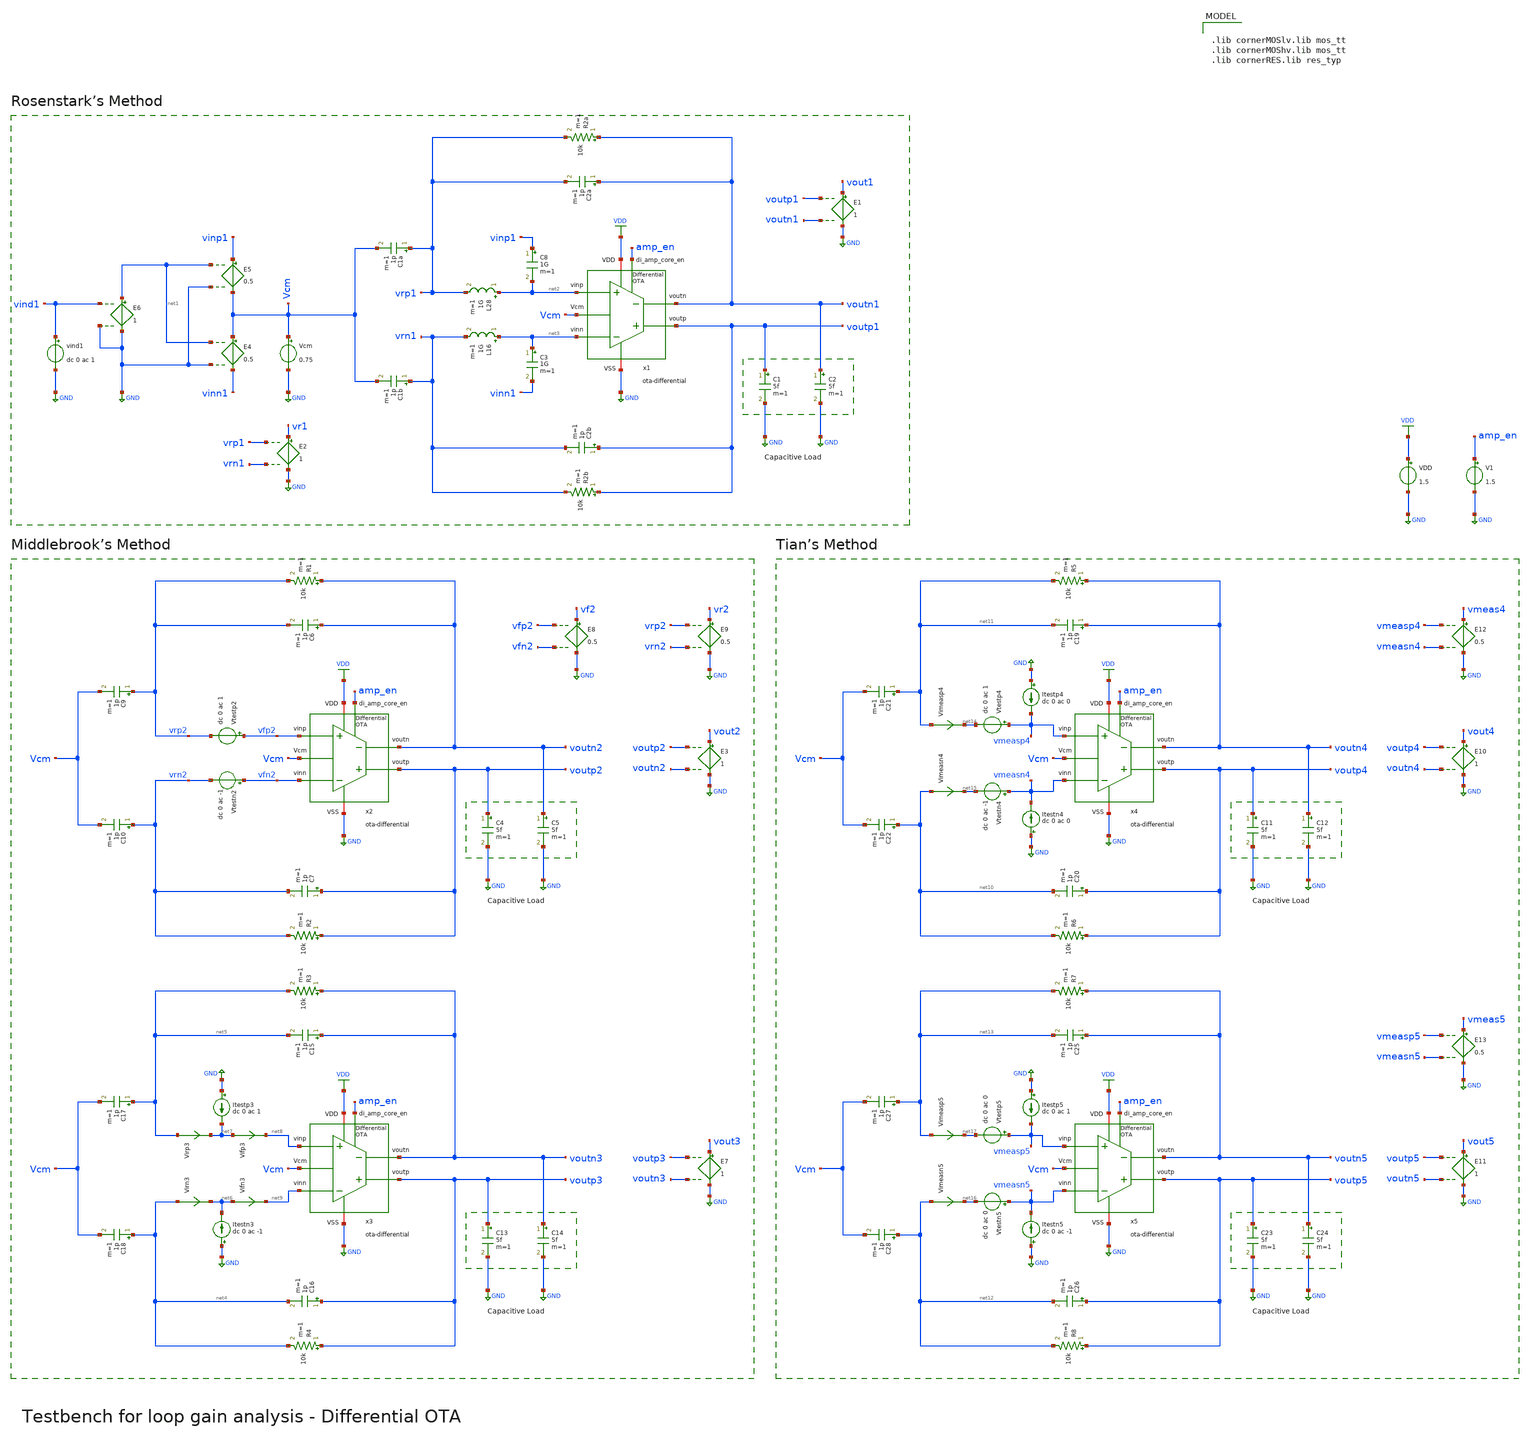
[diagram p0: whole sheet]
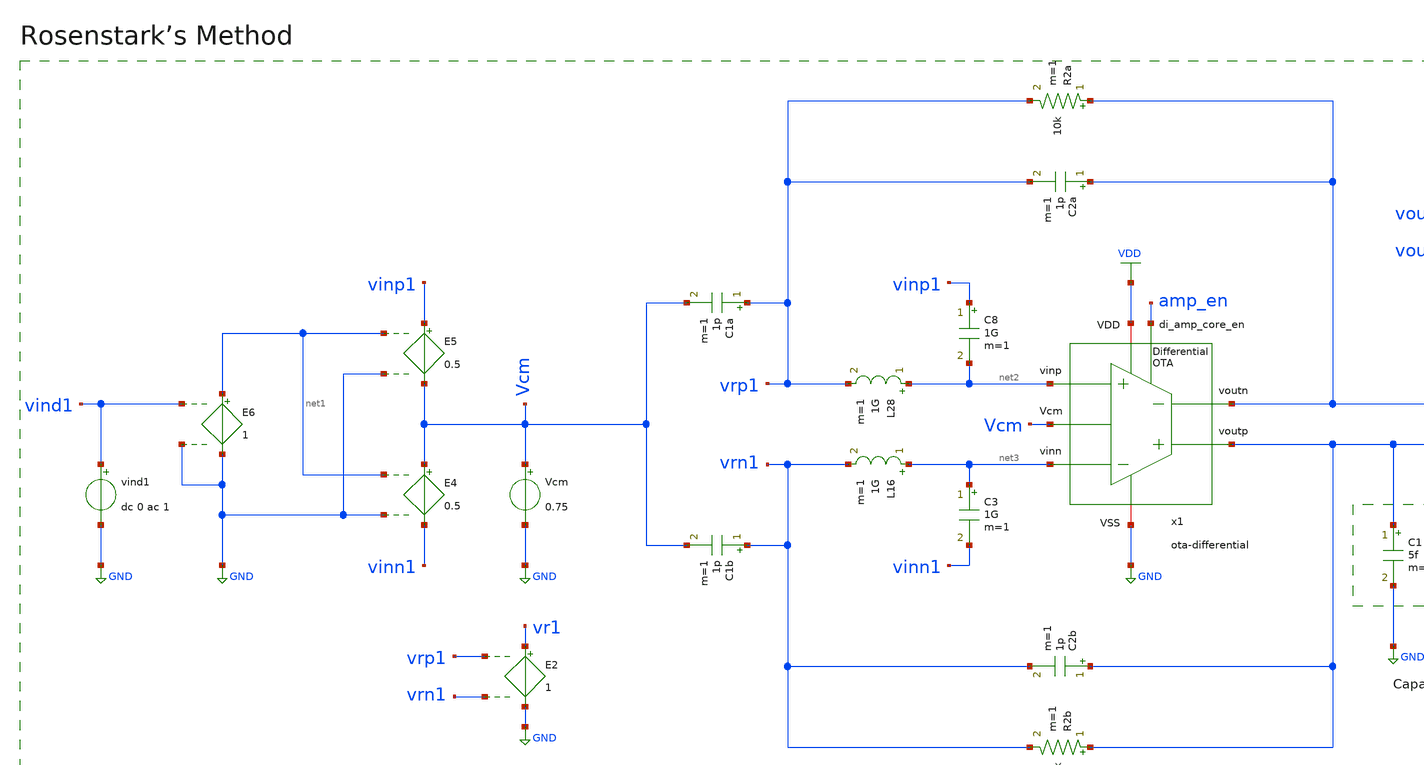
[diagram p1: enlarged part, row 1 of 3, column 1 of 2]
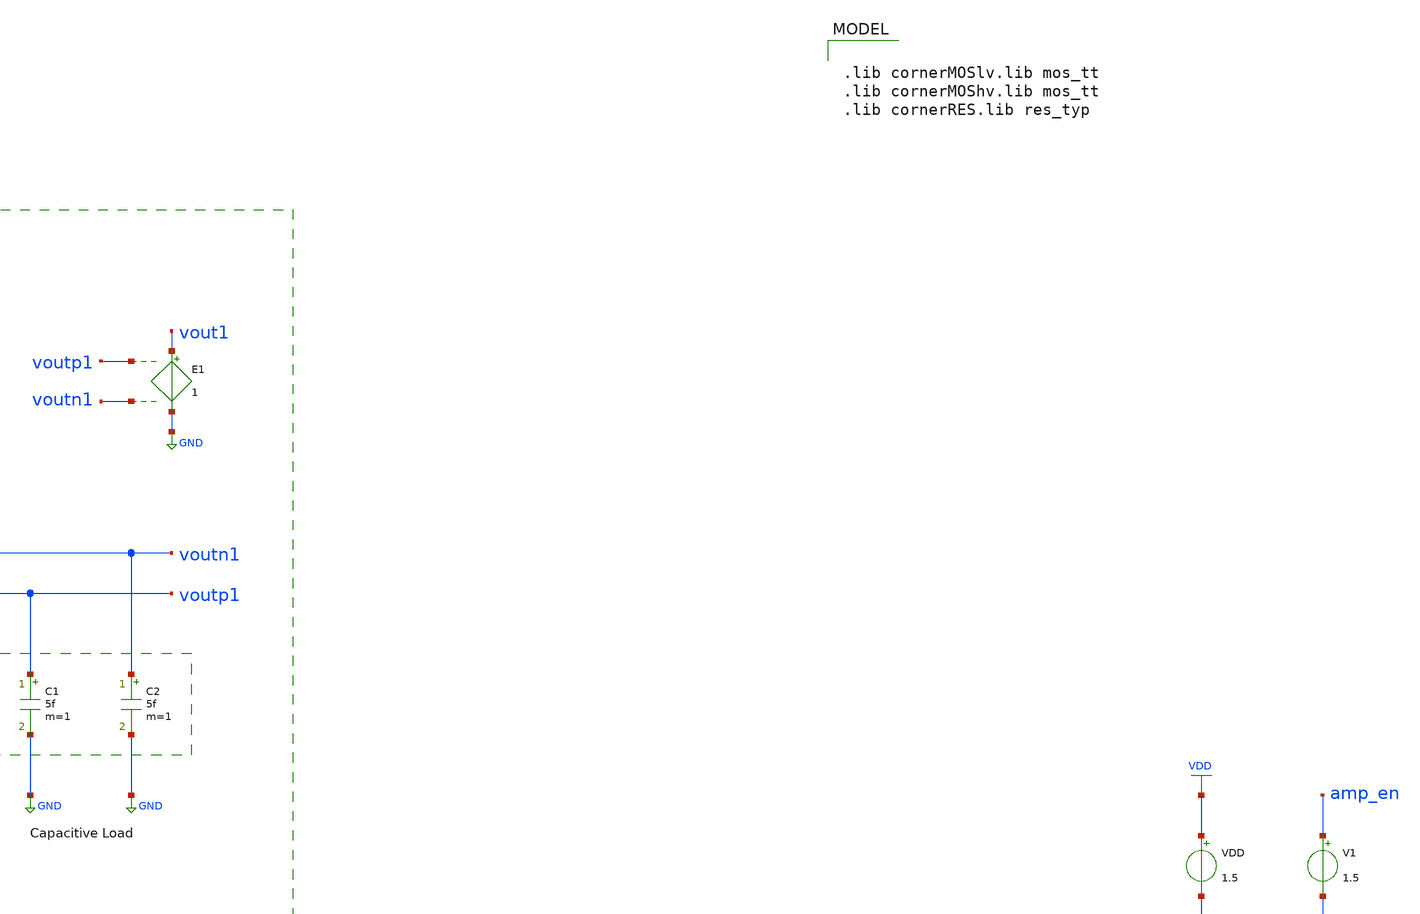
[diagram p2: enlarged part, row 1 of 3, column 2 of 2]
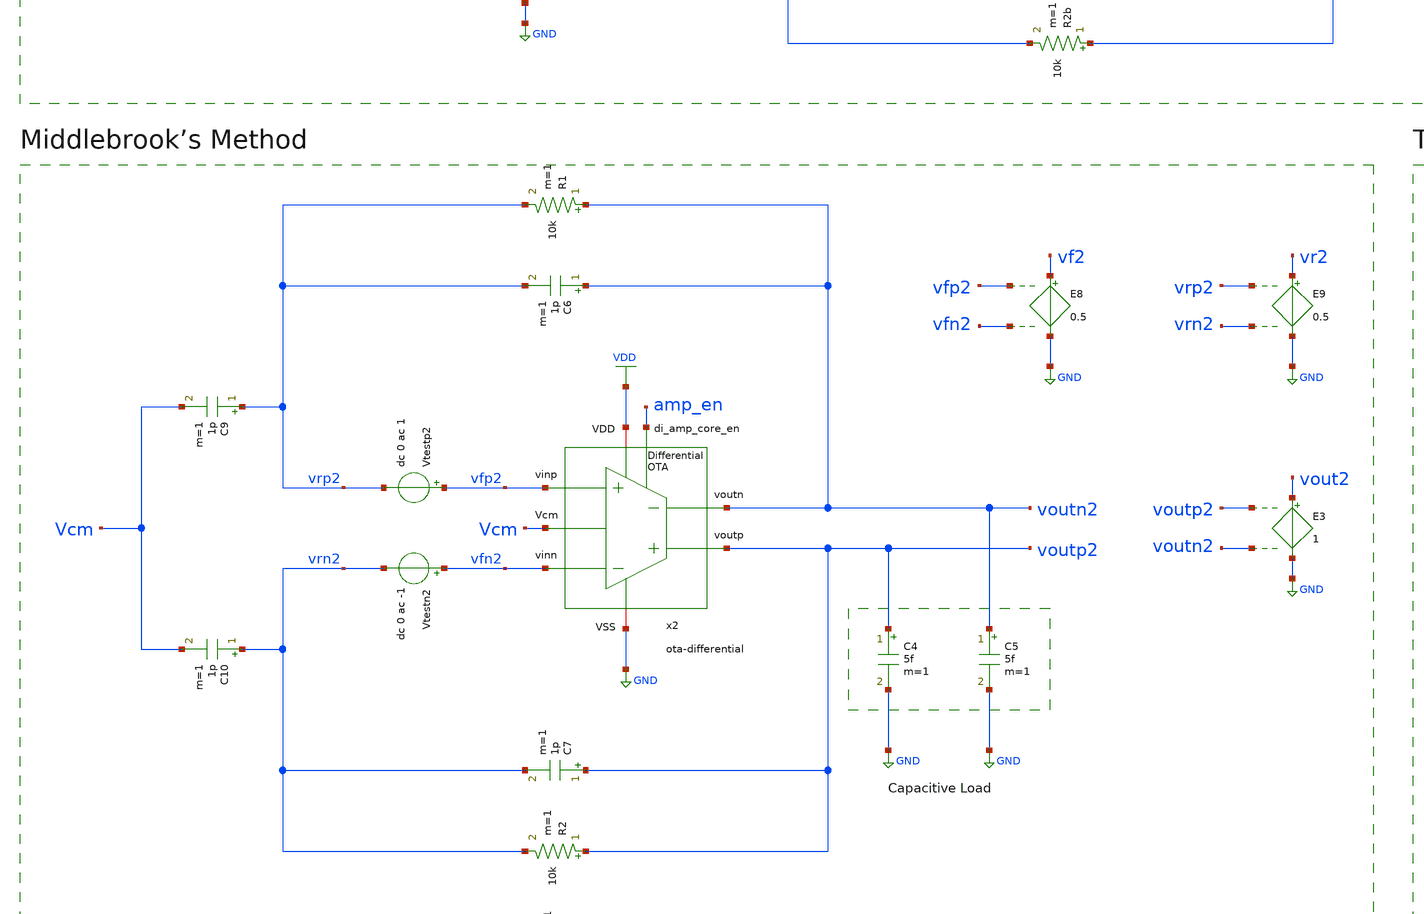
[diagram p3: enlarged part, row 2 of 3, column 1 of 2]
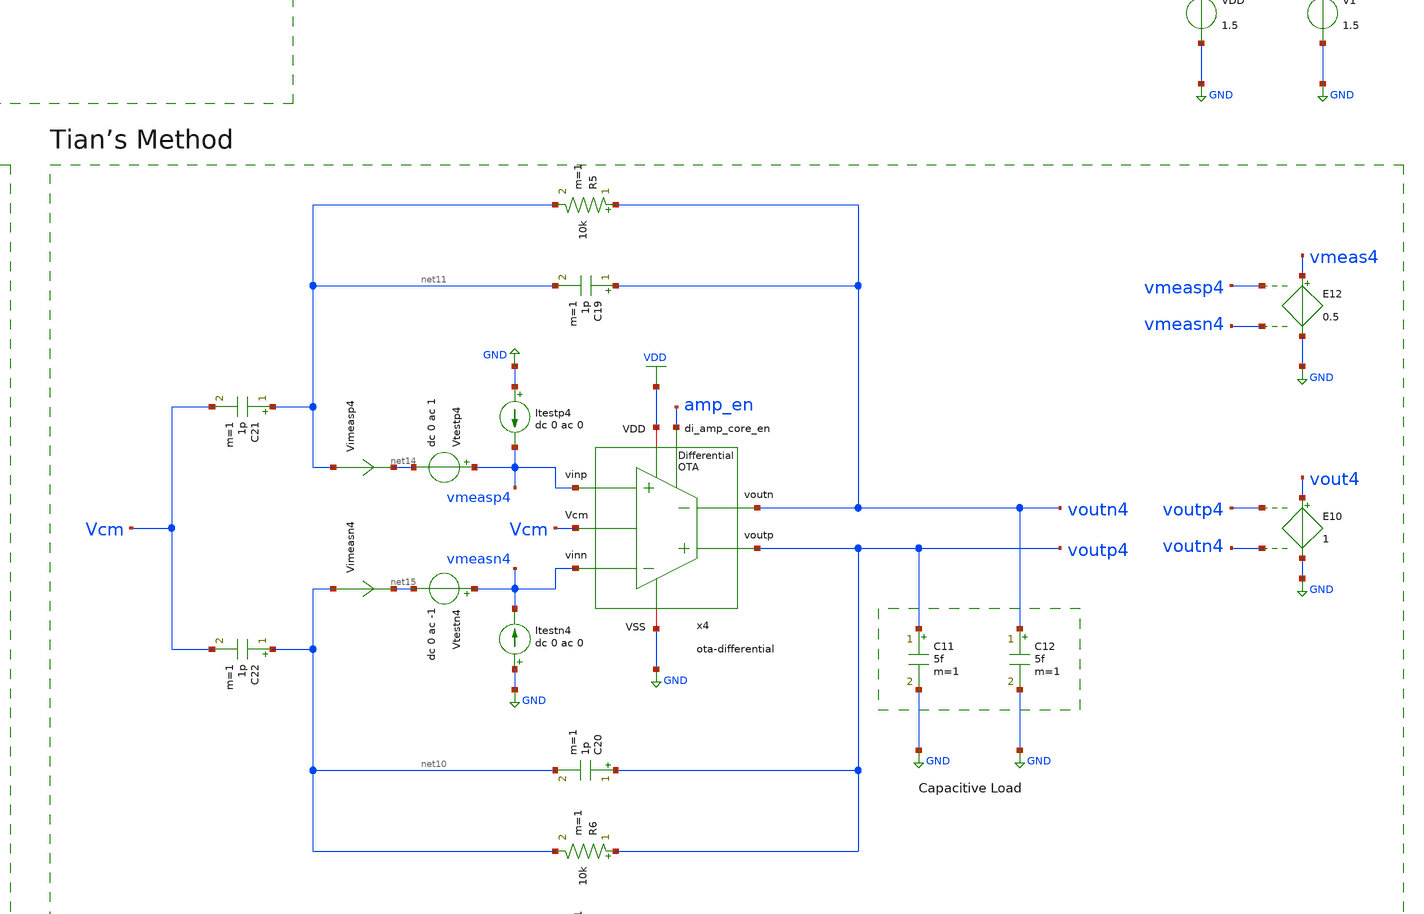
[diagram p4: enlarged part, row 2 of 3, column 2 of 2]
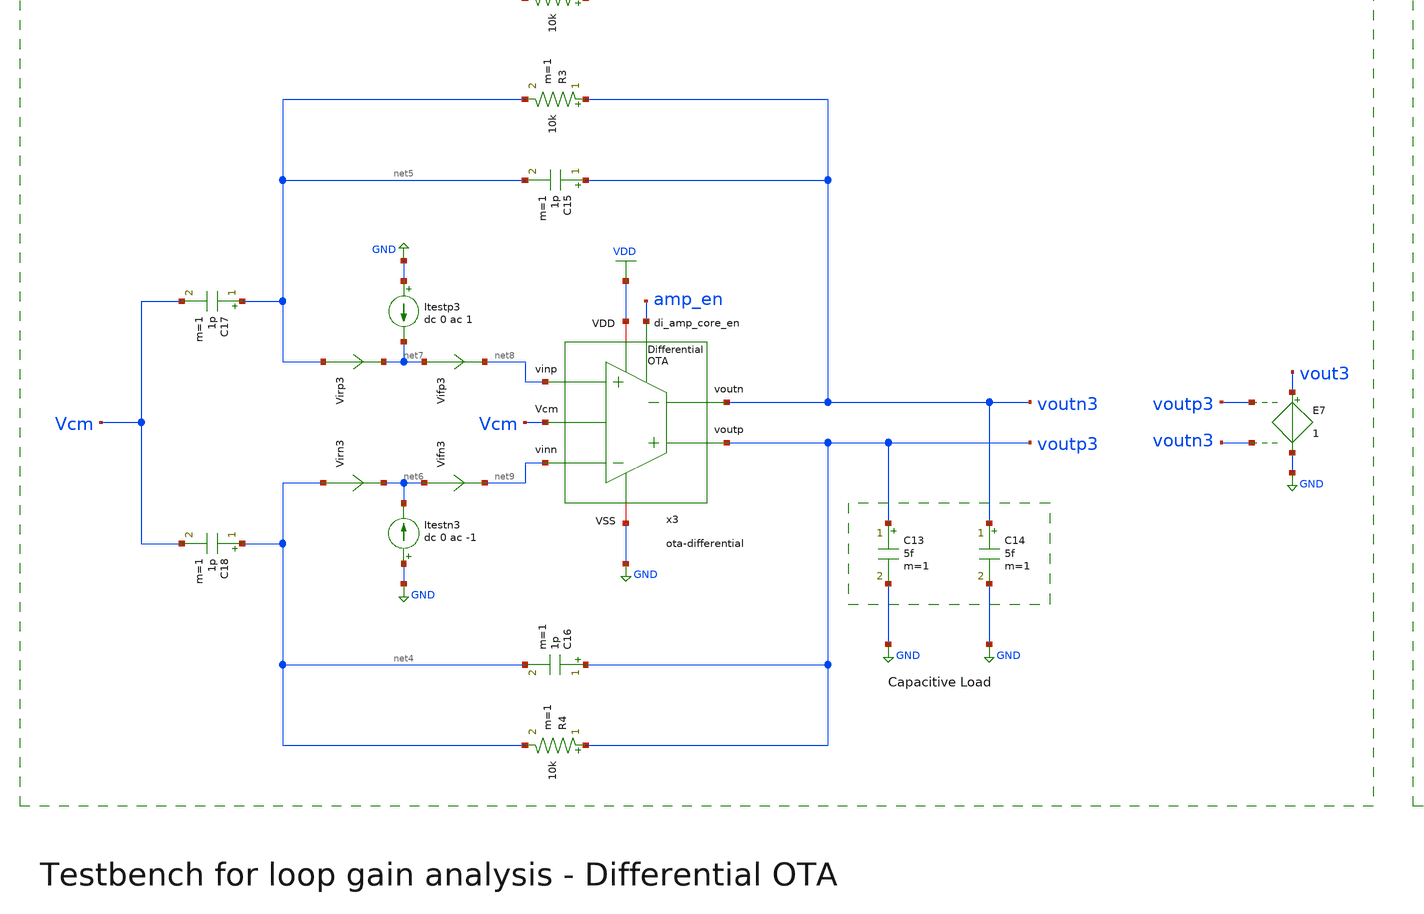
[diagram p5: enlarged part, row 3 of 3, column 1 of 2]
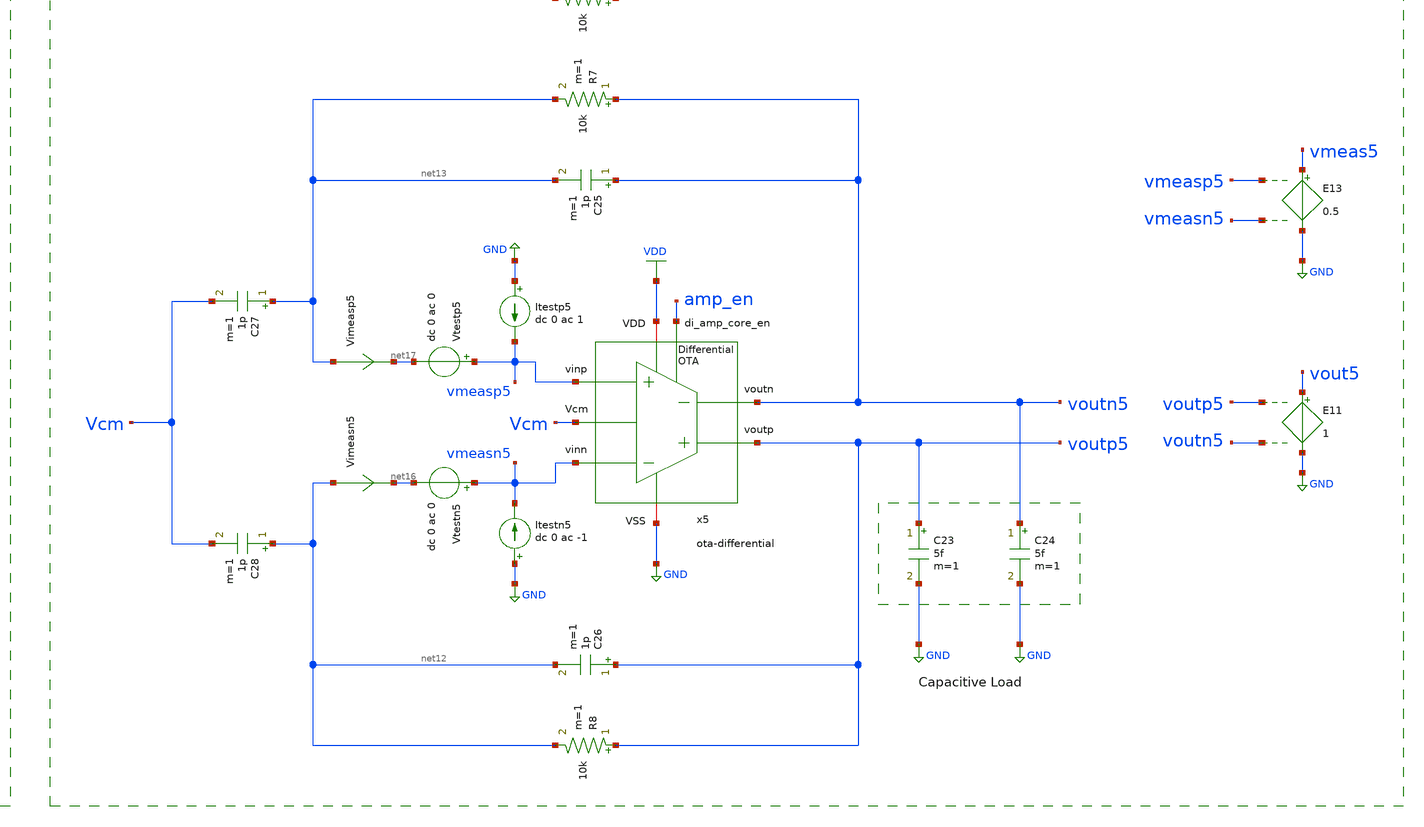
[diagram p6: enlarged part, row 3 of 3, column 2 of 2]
** sch_path: xschem/ota-differential_tb-loopgain.sch
**.subckt ota-differential_tb-loopgain
VDD VDD GND 1.5
C1 voutp1 GND 5f m=1
C2 voutn1 GND 5f m=1
Vcm Vcm GND 0.75
E4 Vcm vinn1 net1 GND 0.5
E5 vinp1 Vcm net1 GND 0.5
E6 net1 GND vind1 GND 1
V1 amp_en GND 1.5
E1 vout1 GND voutp1 voutn1 1
vind1 vind1 GND dc 0 ac 1
R2a voutn1 vrp1 10k m=1
R2b voutp1 vrn1 10k m=1
C2a voutn1 vrp1 1p m=1
C2b voutp1 vrn1 1p m=1
C1a vrp1 Vcm 1p m=1
C1b vrn1 Vcm 1p m=1
C8 vinp1 net2 1G m=1
L28 net2 vrp1 1G m=1
L16 net3 vrn1 1G m=1
C3 net3 vinn1 1G m=1
E2 vr1 GND vrp1 vrn1 1
C4 voutp2 GND 5f m=1
C5 voutn2 GND 5f m=1
E3 vout2 GND voutp2 voutn2 1
R1 voutn2 vrp2 10k m=1
R2 voutp2 vrn2 10k m=1
C6 voutn2 vrp2 1p m=1
C7 voutp2 vrn2 1p m=1
C9 vrp2 Vcm 1p m=1
C10 vrn2 Vcm 1p m=1
C13 voutp3 GND 5f m=1
C14 voutn3 GND 5f m=1
E7 vout3 GND voutp3 voutn3 1
R3 voutn3 net5 10k m=1
R4 voutp3 net4 10k m=1
C15 voutn3 net5 1p m=1
C16 voutp3 net4 1p m=1
C17 net5 Vcm 1p m=1
C18 net4 Vcm 1p m=1
E8 vf2 GND vfp2 vfn2 0.5
E9 vr2 GND vrp2 vrn2 0.5
Vtestp2 vfp2 vrp2 dc 0 ac 1
Vtestn2 vfn2 vrn2 dc 0 ac -1
Virp3 net5 net7 0
.save i(virp3)
Vifp3 net7 net8 0
.save i(vifp3)
Itestn3 GND net6 dc 0 ac -1
Virn3 net4 net6 0
.save i(virn3)
Vifn3 net6 net9 0
.save i(vifn3)
Itestp3 GND net7 dc 0 ac 1
C11 voutp4 GND 5f m=1
C12 voutn4 GND 5f m=1
E10 vout4 GND voutp4 voutn4 1
R5 voutn4 net11 10k m=1
R6 voutp4 net10 10k m=1
C19 voutn4 net11 1p m=1
C20 voutp4 net10 1p m=1
C21 net11 Vcm 1p m=1
C22 net10 Vcm 1p m=1
C23 voutp5 GND 5f m=1
C24 voutn5 GND 5f m=1
E11 vout5 GND voutp5 voutn5 1
R7 voutn5 net13 10k m=1
R8 voutp5 net12 10k m=1
C25 voutn5 net13 1p m=1
C26 voutp5 net12 1p m=1
C27 net13 Vcm 1p m=1
C28 net12 Vcm 1p m=1
Vtestp4 vmeasp4 net14 dc 0 ac 1
Vimeasp4 net11 net14 0
.save i(vimeasp4)
Itestp4 GND vmeasp4 dc 0 ac 0
Vimeasn4 net10 net15 0
.save i(vimeasn4)
Vtestn4 vmeasn4 net15 dc 0 ac -1
Itestn4 GND vmeasn4 dc 0 ac 0
Vimeasn5 net12 net16 0
.save i(vimeasn5)
Vtestn5 vmeasn5 net16 dc 0 ac 0
Itestn5 GND vmeasn5 dc 0 ac -1
Vtestp5 vmeasp5 net17 dc 0 ac 0
Vimeasp5 net13 net17 0
.save i(vimeasp5)
Itestp5 GND vmeasp5 dc 0 ac 1
E12 vmeas4 GND vmeasp4 vmeasn4 0.5
E13 vmeas5 GND vmeasp5 vmeasn5 0.5
x1 voutp1 voutn1 amp_en net3 net2 VDD GND Vcm ota-differential
x2 voutp2 voutn2 amp_en vfn2 vfp2 VDD GND Vcm ota-differential
x3 voutp3 voutn3 amp_en net9 net8 VDD GND Vcm ota-differential
x4 voutp4 voutn4 amp_en vmeasn4 vmeasp4 VDD GND Vcm ota-differential
x5 voutp5 voutn5 amp_en vmeasn5 vmeasp5 VDD GND Vcm ota-differential
**** begin user architecture code

.lib cornerMOSlv.lib mos_tt
.lib cornerMOShv.lib mos_tt
.lib cornerRES.lib res_typ



.param temp=27
.options savecurrents reltol=1e-3 abstol=1e-12 gmin=1e-15
.control
save all

set wr_vecnames
set wr_singlescale

* User Constants
let f_min = 0.01
let f_max = 1G
let fdc = 1
* ===================================================

* Operating Point Analysis
op
remzerovec
write ota-differential_tb-loopgain.raw
set appendwrite
* ===================================================

* AC Analysis
ac dec 101 $&const.f_min $&const.f_max
remzerovec
write ota-differential_tb-loopgain.raw
set appendwrite
* ===================================================

* Rosenstark's method
let L = -v(vr1)/v(vind1)
let L_dB = vdb(L)
let L_arg = 180/PI*cphase(L)

* DC loop gain
meas ac Ldc_dB find L_dB when frequency = fdc
print Ldc_dB

* Phase margin
meas ac fug find frequency when L_dB=0
meas ac pm find L_arg when frequency=fug
let pm = 180-abs(pm)
print pm

* Plotting
plot L_dB L_arg title 'Bode Plot (Rosenstark)' ylabel 'Magnitude (dB), Phase (Deg)'

let L_re = real(L)
let L_im = imag(L)
plot L_im vs L_re retraceplot title 'Nyquist Plot (Rosenstark)' ylabel 'Imaginary Part' xlabel 'Real
+ Part'
* ===================================================

* Middlebrook's method
let Tv=-v(vr2)/v(vf2)
let Ti=-(i(Virp3) - i(Virn3))/(i(Vifp3) - i(Vifn3))
let Tmb =(Tv * Ti - 1)/(Tv + Ti + 2)

let Tmb_dB = vdb(Tmb)
let Tmb_arg = 180/PI*cphase(Tmb)

* DC loop gain
meas ac Tmbdc_dB find Tmb_dB when frequency = fdc
print Tmbdc_dB

* Phase margin
meas ac fug find frequency when Tmb_dB=0
meas ac pm find Tmb_arg when frequency=fug
let pm = 180-abs(pm)
print pm

* Plotting
plot Tmb_dB Tmb_arg title 'Bode Plot (Middlebrook)' ylabel 'Magnitude (dB), Phase (Deg)'

let Tmb_re = real(Tmb)
let Tmb_im = imag(Tmb)
plot Tmb_im vs Tmb_re retraceplot title 'Nyquist Plot (Middlebrook)' ylabel 'Imaginary Part' xlabel 'Real Part'
* ===================================================

* Tian's Method
* vtest=0, itest=1:
let A=i(Vimeasp5)
let C=v(vmeas5)

* vtest=1, itest=0:
let B=i(Vimeasp4)
let D=v(vmeas4)

let Ttian=(A*D-B*C-A)/(2*(B*C-A*D)+A-D+1)

let Ttian_dB = vdb(Ttian)
let Ttian_arg = 180/PI*cphase(Ttian)

* DC loop gain
meas ac Ttianbdc_dB find Ttian_dB when frequency = fdc
print Ttianbdc_dB

* Phase margin
meas ac fug find frequency when Ttian_dB=0
meas ac pm find Ttian_arg when frequency=fug
let pm = 180-abs(pm)
print pm

* Plotting
plot Ttian_dB Ttian_arg title 'Bode Plot (Tian)' ylabel 'Magnitude (dB), Phase (Deg)'

let Ttian_re = real(Ttian)
let Ttian_im = imag(Ttian)
plot Ttian_im vs Ttian_re retraceplot title 'Nyquist Plot (Tian)' ylabel 'Imaginary Part' xlabel 'Real
+ Part'
* ===================================================

* Rosenstark vs. Middlebrook vs. Tian
plot L_dB Tmb_dB Ttian_dB title 'Rosenstark vs. Middlebrook vs. Tian' ylabel 'Magnitude (dB)'
plot L_arg Tmb_arg Ttian_arg title 'Rosenstark vs. Middlebrook vs. Tian' ylabel 'Phase (Deg)'

* plot L_im vs L_re Tmb_im vs Tmb_re Ttian_im vs Ttian_re retraceplot title 'Rosenstark vs. Middlebrook
*+ vs. Tian' ylabel 'Imaginary Part' xlabel 'Real Part'
plot Tmb_im vs Tmb_re Ttian_im vs Ttian_re retraceplot title 'Middlebrook vs. Tian' ylabel 'Imaginary
+ Part' xlabel 'Real Part'
* ===================================================

*quit
.endc


**** end user architecture code
**.ends
.GLOBAL GND
.GLOBAL VDD
.end
